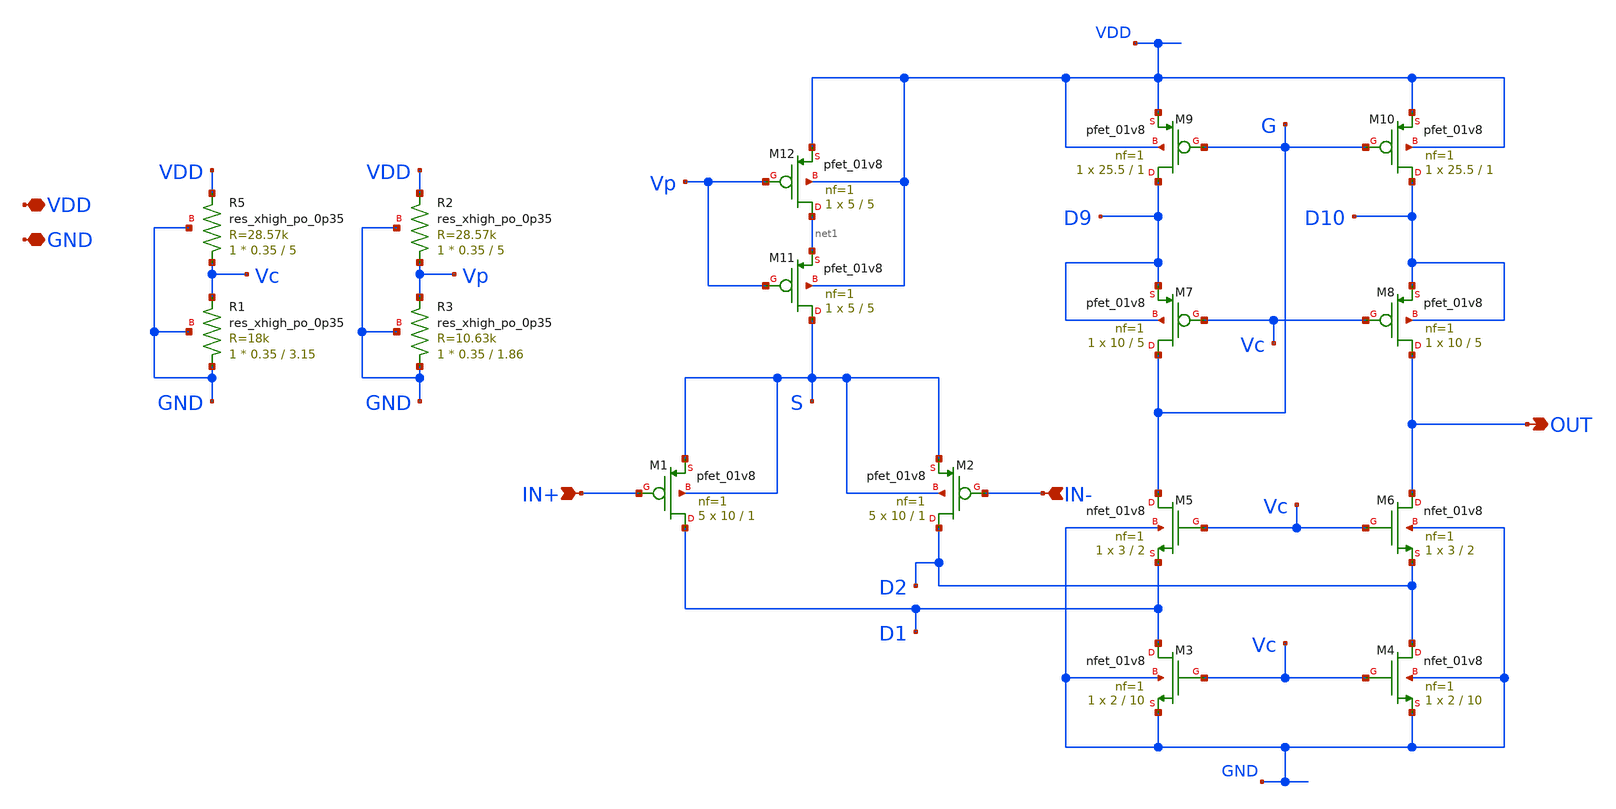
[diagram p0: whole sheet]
** sch_path: xschem/tt10_FoldedCascode.sch
**.subckt tt10_FoldedCascode VDD GND IN+ IN- OUT
*.iopin VDD
*.iopin GND
*.ipin IN+
*.ipin IN-
*.opin OUT
XM1 D1 IN+ S S sky130_fd_pr__pfet_01v8 L=1 W=10 nf=1 ad='int((nf+1)/2) * W/nf * 0.29' as='int((nf+2)/2) * W/nf * 0.29'
+ pd='2*int((nf+1)/2) * (W/nf + 0.29)' ps='2*int((nf+2)/2) * (W/nf + 0.29)' nrd='0.29 / W' nrs='0.29 / W'
+ sa=0 sb=0 sd=0 mult=5 m=5
XM2 D2 IN- S S sky130_fd_pr__pfet_01v8 L=1 W=10 nf=1 ad='int((nf+1)/2) * W/nf * 0.29' as='int((nf+2)/2) * W/nf * 0.29'
+ pd='2*int((nf+1)/2) * (W/nf + 0.29)' ps='2*int((nf+2)/2) * (W/nf + 0.29)' nrd='0.29 / W' nrs='0.29 / W'
+ sa=0 sb=0 sd=0 mult=5 m=5
XM3 D1 Vc GND GND sky130_fd_pr__nfet_01v8 L=10 W=2 nf=1 ad='int((nf+1)/2) * W/nf * 0.29' as='int((nf+2)/2) * W/nf * 0.29'
+ pd='2*int((nf+1)/2) * (W/nf + 0.29)' ps='2*int((nf+2)/2) * (W/nf + 0.29)' nrd='0.29 / W' nrs='0.29 / W'
+ sa=0 sb=0 sd=0 mult=1 m=1
XM4 D2 Vc GND GND sky130_fd_pr__nfet_01v8 L=10 W=2 nf=1 ad='int((nf+1)/2) * W/nf * 0.29' as='int((nf+2)/2) * W/nf * 0.29'
+ pd='2*int((nf+1)/2) * (W/nf + 0.29)' ps='2*int((nf+2)/2) * (W/nf + 0.29)' nrd='0.29 / W' nrs='0.29 / W'
+ sa=0 sb=0 sd=0 mult=1 m=1
XM5 G Vc D1 GND sky130_fd_pr__nfet_01v8 L=2 W=3 nf=1 ad='int((nf+1)/2) * W/nf * 0.29' as='int((nf+2)/2) * W/nf * 0.29'
+ pd='2*int((nf+1)/2) * (W/nf + 0.29)' ps='2*int((nf+2)/2) * (W/nf + 0.29)' nrd='0.29 / W' nrs='0.29 / W'
+ sa=0 sb=0 sd=0 mult=1 m=1
XM6 OUT Vc D2 GND sky130_fd_pr__nfet_01v8 L=2 W=3 nf=1 ad='int((nf+1)/2) * W/nf * 0.29' as='int((nf+2)/2) * W/nf * 0.29'
+ pd='2*int((nf+1)/2) * (W/nf + 0.29)' ps='2*int((nf+2)/2) * (W/nf + 0.29)' nrd='0.29 / W' nrs='0.29 / W'
+ sa=0 sb=0 sd=0 mult=1 m=1
XM7 G Vc D9 D9 sky130_fd_pr__pfet_01v8 L=5 W=10 nf=1 ad='int((nf+1)/2) * W/nf * 0.29' as='int((nf+2)/2) * W/nf * 0.29'
+ pd='2*int((nf+1)/2) * (W/nf + 0.29)' ps='2*int((nf+2)/2) * (W/nf + 0.29)' nrd='0.29 / W' nrs='0.29 / W'
+ sa=0 sb=0 sd=0 mult=1 m=1
XM8 OUT Vc D10 D10 sky130_fd_pr__pfet_01v8 L=5 W=10 nf=1 ad='int((nf+1)/2) * W/nf * 0.29' as='int((nf+2)/2) * W/nf * 0.29'
+ pd='2*int((nf+1)/2) * (W/nf + 0.29)' ps='2*int((nf+2)/2) * (W/nf + 0.29)' nrd='0.29 / W' nrs='0.29 / W'
+ sa=0 sb=0 sd=0 mult=1 m=1
XM9 D9 G VDD VDD sky130_fd_pr__pfet_01v8 L=1 W=25.5 nf=1 ad='int((nf+1)/2) * W/nf * 0.29' as='int((nf+2)/2) * W/nf * 0.29'
+ pd='2*int((nf+1)/2) * (W/nf + 0.29)' ps='2*int((nf+2)/2) * (W/nf + 0.29)' nrd='0.29 / W' nrs='0.29 / W'
+ sa=0 sb=0 sd=0 mult=1 m=1
XM10 D10 G VDD VDD sky130_fd_pr__pfet_01v8 L=1 W=25.5 nf=1 ad='int((nf+1)/2) * W/nf * 0.29' as='int((nf+2)/2) * W/nf * 0.29'
+ pd='2*int((nf+1)/2) * (W/nf + 0.29)' ps='2*int((nf+2)/2) * (W/nf + 0.29)' nrd='0.29 / W' nrs='0.29 / W'
+ sa=0 sb=0 sd=0 mult=1 m=1
XM11 S Vp net1 VDD sky130_fd_pr__pfet_01v8 L=5 W=5 nf=1 ad='int((nf+1)/2) * W/nf * 0.29' as='int((nf+2)/2) * W/nf * 0.29'
+ pd='2*int((nf+1)/2) * (W/nf + 0.29)' ps='2*int((nf+2)/2) * (W/nf + 0.29)' nrd='0.29 / W' nrs='0.29 / W'
+ sa=0 sb=0 sd=0 mult=1 m=1
XM12 net1 Vp VDD VDD sky130_fd_pr__pfet_01v8 L=5 W=5 nf=1 ad='int((nf+1)/2) * W/nf * 0.29' as='int((nf+2)/2) * W/nf * 0.29'
+ pd='2*int((nf+1)/2) * (W/nf + 0.29)' ps='2*int((nf+2)/2) * (W/nf + 0.29)' nrd='0.29 / W' nrs='0.29 / W'
+ sa=0 sb=0 sd=0 mult=1 m=1
XR5 Vc VDD GND sky130_fd_pr__res_xhigh_po_0p35 L=5 mult=1 m=1
XR1 GND Vc GND sky130_fd_pr__res_xhigh_po_0p35 L=3.15 mult=1 m=1
XR2 Vp VDD GND sky130_fd_pr__res_xhigh_po_0p35 L=5 mult=1 m=1
XR3 GND Vp GND sky130_fd_pr__res_xhigh_po_0p35 L=1.86 mult=1 m=1
**.ends
.end
